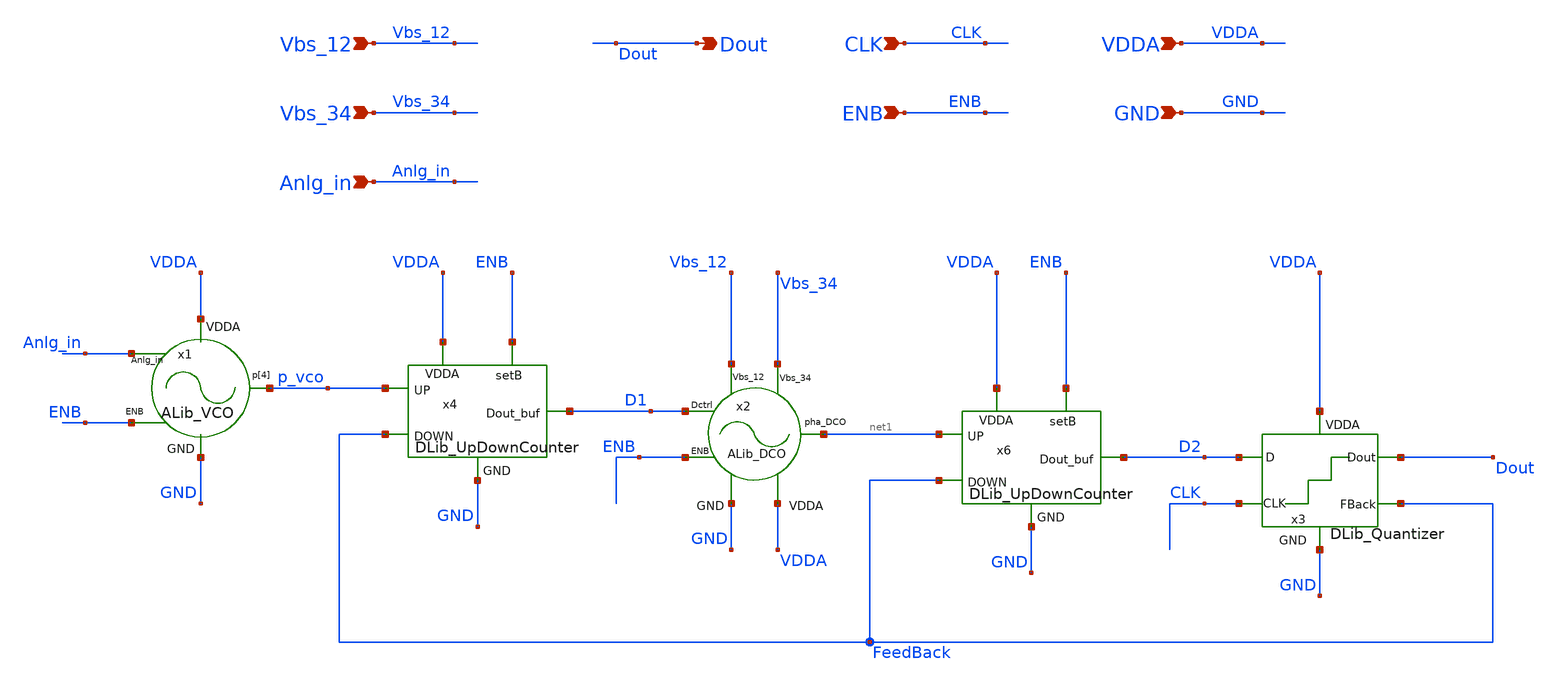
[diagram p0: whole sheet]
** sch_path: xschem/lib/ALib_VCO_ADC2.sch
**.subckt ALib_VCO_ADC2 VDDA Dout GND ENB CLK Vbs_34 Anlg_in Vbs_12
*.ipin VDDA
*.opin Dout
*.ipin GND
*.ipin ENB
*.ipin CLK
*.ipin Vbs_34
*.ipin Anlg_in
*.ipin Vbs_12
x1 Anlg_in ENB p_vco VDDA GND ALib_VCO
x2 Vbs_12 Vbs_34 net1 D1 ENB VDDA GND ALib_DCO
x3 D2 CLK Dout FeedBack VDDA GND DLib_Quantizer
x4 p_vco FeedBack ENB D1 VDDA GND DLib_UpDownCounter
x6 net1 FeedBack ENB D2 VDDA GND DLib_UpDownCounter
**.ends
.end
